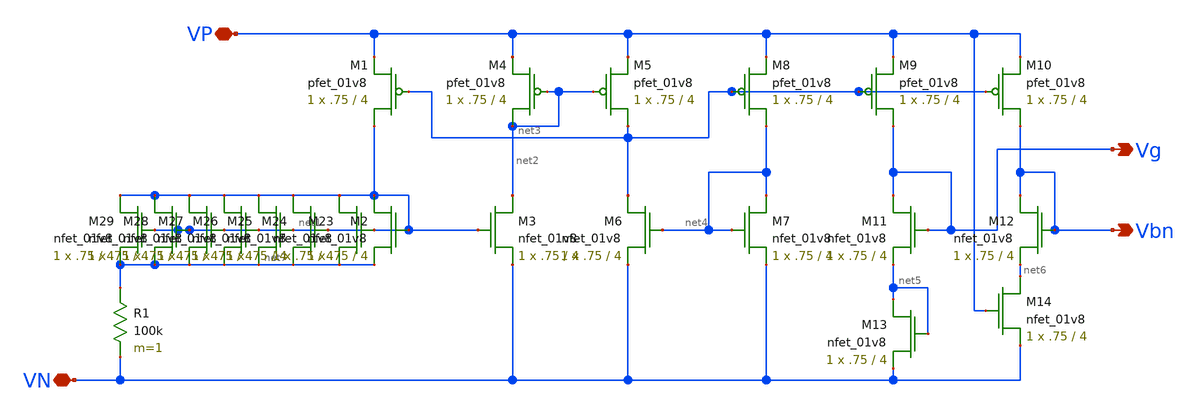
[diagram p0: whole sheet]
** sch_path: VoltageGenerator.sch
**.subckt VoltageGenerator VP VN Vg Vbn
*.iopin VP
*.iopin VN
*.opin Vg
*.opin Vbn
XM1 net1 net3 VP VDD sky130_fd_pr__pfet_01v8 L=4 W=.75 nf=1 ad='int((nf+1)/2) * W/nf * 0.29' as='int((nf+2)/2) * W/nf * 0.29'
+ pd='2*int((nf+1)/2) * (W/nf + 0.29)' ps='2*int((nf+2)/2) * (W/nf + 0.29)' nrd='0.29 / W' nrs='0.29 / W'
+ sa=0 sb=0 sd=0 mult=1 m=1
XM2 net1 net1 net7 GND sky130_fd_pr__nfet_01v8 L=4 W=.75 nf=1 ad='int((nf+1)/2) * W/nf * 0.29' as='int((nf+2)/2) * W/nf * 0.29'
+ pd='2*int((nf+1)/2) * (W/nf + 0.29)' ps='2*int((nf+2)/2) * (W/nf + 0.29)' nrd='0.29 / W' nrs='0.29 / W'
+ sa=0 sb=0 sd=0 mult=1 m=1
XM3 net2 net1 VN GND sky130_fd_pr__nfet_01v8 L=4 W=.75 nf=1 ad='int((nf+1)/2) * W/nf * 0.29' as='int((nf+2)/2) * W/nf * 0.29'
+ pd='2*int((nf+1)/2) * (W/nf + 0.29)' ps='2*int((nf+2)/2) * (W/nf + 0.29)' nrd='0.29 / W' nrs='0.29 / W'
+ sa=0 sb=0 sd=0 mult=1 m=1
XM4 net2 net2 VP VDD sky130_fd_pr__pfet_01v8 L=4 W=.75 nf=1 ad='int((nf+1)/2) * W/nf * 0.29' as='int((nf+2)/2) * W/nf * 0.29'
+ pd='2*int((nf+1)/2) * (W/nf + 0.29)' ps='2*int((nf+2)/2) * (W/nf + 0.29)' nrd='0.29 / W' nrs='0.29 / W'
+ sa=0 sb=0 sd=0 mult=1 m=1
R1 net7 VN 100k m=1
XM5 net3 net2 VP VDD sky130_fd_pr__pfet_01v8 L=4 W=.75 nf=1 ad='int((nf+1)/2) * W/nf * 0.29' as='int((nf+2)/2) * W/nf * 0.29'
+ pd='2*int((nf+1)/2) * (W/nf + 0.29)' ps='2*int((nf+2)/2) * (W/nf + 0.29)' nrd='0.29 / W' nrs='0.29 / W'
+ sa=0 sb=0 sd=0 mult=1 m=1
XM6 net3 net4 VN GND sky130_fd_pr__nfet_01v8 L=4 W=.75 nf=1 ad='int((nf+1)/2) * W/nf * 0.29' as='int((nf+2)/2) * W/nf * 0.29'
+ pd='2*int((nf+1)/2) * (W/nf + 0.29)' ps='2*int((nf+2)/2) * (W/nf + 0.29)' nrd='0.29 / W' nrs='0.29 / W'
+ sa=0 sb=0 sd=0 mult=1 m=1
XM7 net4 net4 VN GND sky130_fd_pr__nfet_01v8 L=4 W=.75 nf=1 ad='int((nf+1)/2) * W/nf * 0.29' as='int((nf+2)/2) * W/nf * 0.29'
+ pd='2*int((nf+1)/2) * (W/nf + 0.29)' ps='2*int((nf+2)/2) * (W/nf + 0.29)' nrd='0.29 / W' nrs='0.29 / W'
+ sa=0 sb=0 sd=0 mult=1 m=1
XM8 net4 net3 VP VDD sky130_fd_pr__pfet_01v8 L=4 W=.75 nf=1 ad='int((nf+1)/2) * W/nf * 0.29' as='int((nf+2)/2) * W/nf * 0.29'
+ pd='2*int((nf+1)/2) * (W/nf + 0.29)' ps='2*int((nf+2)/2) * (W/nf + 0.29)' nrd='0.29 / W' nrs='0.29 / W'
+ sa=0 sb=0 sd=0 mult=1 m=1
XM9 Vg net3 VP VDD sky130_fd_pr__pfet_01v8 L=4 W=.75 nf=1 ad='int((nf+1)/2) * W/nf * 0.29' as='int((nf+2)/2) * W/nf * 0.29'
+ pd='2*int((nf+1)/2) * (W/nf + 0.29)' ps='2*int((nf+2)/2) * (W/nf + 0.29)' nrd='0.29 / W' nrs='0.29 / W'
+ sa=0 sb=0 sd=0 mult=1 m=1
XM10 Vbn net3 VP VDD sky130_fd_pr__pfet_01v8 L=4 W=.75 nf=1 ad='int((nf+1)/2) * W/nf * 0.29' as='int((nf+2)/2) * W/nf * 0.29'
+ pd='2*int((nf+1)/2) * (W/nf + 0.29)' ps='2*int((nf+2)/2) * (W/nf + 0.29)' nrd='0.29 / W' nrs='0.29 / W'
+ sa=0 sb=0 sd=0 mult=1 m=1
XM11 Vg Vg net5 GND sky130_fd_pr__nfet_01v8 L=4 W=.75 nf=1 ad='int((nf+1)/2) * W/nf * 0.29' as='int((nf+2)/2) * W/nf * 0.29'
+ pd='2*int((nf+1)/2) * (W/nf + 0.29)' ps='2*int((nf+2)/2) * (W/nf + 0.29)' nrd='0.29 / W' nrs='0.29 / W'
+ sa=0 sb=0 sd=0 mult=1 m=1
XM12 Vbn Vbn net6 GND sky130_fd_pr__nfet_01v8 L=4 W=.75 nf=1 ad='int((nf+1)/2) * W/nf * 0.29' as='int((nf+2)/2) * W/nf * 0.29'
+ pd='2*int((nf+1)/2) * (W/nf + 0.29)' ps='2*int((nf+2)/2) * (W/nf + 0.29)' nrd='0.29 / W' nrs='0.29 / W'
+ sa=0 sb=0 sd=0 mult=1 m=1
XM13 net5 net5 VN GND sky130_fd_pr__nfet_01v8 L=4 W=.75 nf=1 ad='int((nf+1)/2) * W/nf * 0.29' as='int((nf+2)/2) * W/nf * 0.29'
+ pd='2*int((nf+1)/2) * (W/nf + 0.29)' ps='2*int((nf+2)/2) * (W/nf + 0.29)' nrd='0.29 / W' nrs='0.29 / W'
+ sa=0 sb=0 sd=0 mult=1 m=1
XM14 net6 VP VN GND sky130_fd_pr__nfet_01v8 L=4 W=.75 nf=1 ad='int((nf+1)/2) * W/nf * 0.29' as='int((nf+2)/2) * W/nf * 0.29'
+ pd='2*int((nf+1)/2) * (W/nf + 0.29)' ps='2*int((nf+2)/2) * (W/nf + 0.29)' nrd='0.29 / W' nrs='0.29 / W'
+ sa=0 sb=0 sd=0 mult=1 m=1
XM23 net1 net1 net7 GND sky130_fd_pr__nfet_01v8 L=4 W=.75 nf=1 ad='int((nf+1)/2) * W/nf * 0.29' as='int((nf+2)/2) * W/nf * 0.29'
+ pd='2*int((nf+1)/2) * (W/nf + 0.29)' ps='2*int((nf+2)/2) * (W/nf + 0.29)' nrd='0.29 / W' nrs='0.29 / W'
+ sa=0 sb=0 sd=0 mult=1 m=1
XM24 net1 net1 net7 GND sky130_fd_pr__nfet_01v8 L=4 W=.75 nf=1 ad='int((nf+1)/2) * W/nf * 0.29' as='int((nf+2)/2) * W/nf * 0.29'
+ pd='2*int((nf+1)/2) * (W/nf + 0.29)' ps='2*int((nf+2)/2) * (W/nf + 0.29)' nrd='0.29 / W' nrs='0.29 / W'
+ sa=0 sb=0 sd=0 mult=1 m=1
XM25 net1 net1 net7 GND sky130_fd_pr__nfet_01v8 L=4 W=.75 nf=1 ad='int((nf+1)/2) * W/nf * 0.29' as='int((nf+2)/2) * W/nf * 0.29'
+ pd='2*int((nf+1)/2) * (W/nf + 0.29)' ps='2*int((nf+2)/2) * (W/nf + 0.29)' nrd='0.29 / W' nrs='0.29 / W'
+ sa=0 sb=0 sd=0 mult=1 m=1
XM26 net1 net1 net7 GND sky130_fd_pr__nfet_01v8 L=4 W=.75 nf=1 ad='int((nf+1)/2) * W/nf * 0.29' as='int((nf+2)/2) * W/nf * 0.29'
+ pd='2*int((nf+1)/2) * (W/nf + 0.29)' ps='2*int((nf+2)/2) * (W/nf + 0.29)' nrd='0.29 / W' nrs='0.29 / W'
+ sa=0 sb=0 sd=0 mult=1 m=1
XM27 net1 net1 net7 GND sky130_fd_pr__nfet_01v8 L=4 W=.75 nf=1 ad='int((nf+1)/2) * W/nf * 0.29' as='int((nf+2)/2) * W/nf * 0.29'
+ pd='2*int((nf+1)/2) * (W/nf + 0.29)' ps='2*int((nf+2)/2) * (W/nf + 0.29)' nrd='0.29 / W' nrs='0.29 / W'
+ sa=0 sb=0 sd=0 mult=1 m=1
XM28 net1 net1 net7 GND sky130_fd_pr__nfet_01v8 L=4 W=.75 nf=1 ad='int((nf+1)/2) * W/nf * 0.29' as='int((nf+2)/2) * W/nf * 0.29'
+ pd='2*int((nf+1)/2) * (W/nf + 0.29)' ps='2*int((nf+2)/2) * (W/nf + 0.29)' nrd='0.29 / W' nrs='0.29 / W'
+ sa=0 sb=0 sd=0 mult=1 m=1
XM29 net1 net1 net7 GND sky130_fd_pr__nfet_01v8 L=4 W=.75 nf=1 ad='int((nf+1)/2) * W/nf * 0.29' as='int((nf+2)/2) * W/nf * 0.29'
+ pd='2*int((nf+1)/2) * (W/nf + 0.29)' ps='2*int((nf+2)/2) * (W/nf + 0.29)' nrd='0.29 / W' nrs='0.29 / W'
+ sa=0 sb=0 sd=0 mult=1 m=1
**.ends
.end
